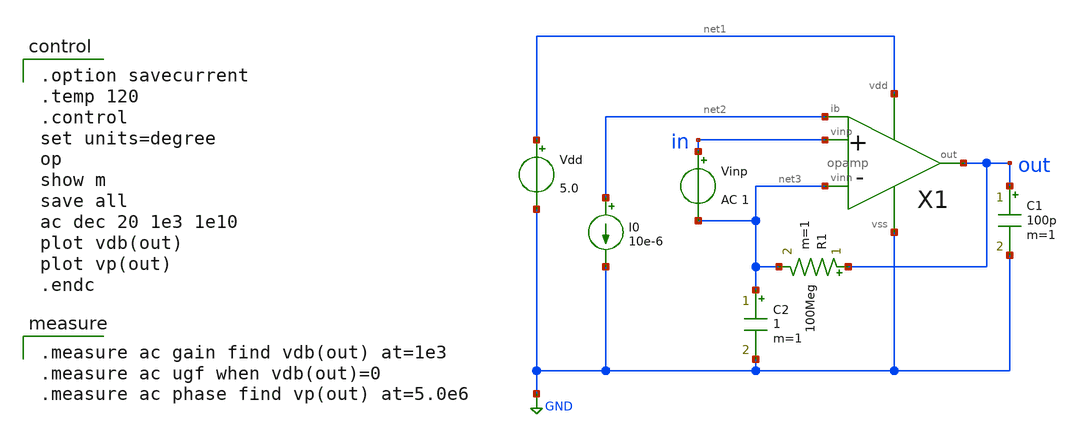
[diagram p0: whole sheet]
** sch_path: schematic/20250924_OSS_Workshop/ishikai/opamp/sample/opamp_ac_temp.sch
**.subckt opamp_ac_temp
Vdd net1 GND 5.0
C1 out GND 100p m=1
X1 in net3 net2 out net1 GND opamp
I0 net2 GND 10e-6
R1 out net3 100Meg m=1
C2 net3 GND 1 m=1
Vinp in net3 AC 1
**** begin user architecture code

.option savecurrent
.temp 120
.control
set units=degree
op
show m
save all
ac dec 20 1e3 1e10
plot vdb(out)
plot vp(out)
.endc


.measure ac gain find vdb(out) at=1e3
.measure ac ugf when vdb(out)=0
.measure ac phase find vp(out) at=5.0e6

 .include $::LIB/../ip62_models
**** end user architecture code
**.ends

* expanding   symbol:  opamp.sym # of pins=6
** sym_path: schematic/20250924_OSS_Workshop/ishikai/opamp/sample/opamp.sym
** sch_path: schematic/20250924_OSS_Workshop/ishikai/opamp/sample/opamp.sch
.subckt opamp vinp vinn ib out vdd vss
*.ipin vinp
*.ipin vinn
*.opin out
*.iopin vdd
*.iopin vss
*.iopin ib
X1 vinp vinn net2 vdd vss ib diff
X2 net2 ib out vdd vss cs
XM9 net1 ib vdd vdd PMOS w=30u l=1u as=0 ad=0 ps=0 pd=0 nrd=0 nrs=0 m=1
XM12 net3 net1 net2 vss NMOS w=20u l=1u as=0 ad=0 ps=0 pd=0 nrd=0 nrs=0 m=1
XM1 ib ib vdd vdd PMOS w=30u l=1u as=0 ad=0 ps=0 pd=0 nrd=0 nrs=0 m=1
XM10 net1 net1 net4 vss NMOS w=10u l=1u as=0 ad=0 ps=0 pd=0 nrd=0 nrs=0 m=1
XM11 net4 net4 vss vss NMOS w=10u l=1u as=0 ad=0 ps=0 pd=0 nrd=0 nrs=0 m=1
XC1 net3 out vss F_CSIO c=8.856p x=120u y=120u m=1
.ends


* expanding   symbol:  diff.sym # of pins=6
** sym_path: schematic/20250924_OSS_Workshop/ishikai/opamp/sample/diff.sym
** sch_path: schematic/20250924_OSS_Workshop/ishikai/opamp/sample/diff.sch
.subckt diff vinp vinn out vdd vss vb
*.ipin vinn
*.ipin vinp
*.ipin vb
*.opin out
*.iopin vdd
*.iopin vss
XM5 net2 vb vdd vdd PMOS w=180u l=1u as=0 ad=0 ps=0 pd=0 nrd=0 nrs=0 m=1
XM1 net1 vinn net2 net2 PMOS w=360u l=1u as=0 ad=0 ps=0 pd=0 nrd=0 nrs=0 m=1
XM2 out vinp net2 net2 PMOS w=360u l=1u as=0 ad=0 ps=0 pd=0 nrd=0 nrs=0 m=1
XM3 net1 net1 vss vss NMOS w=30u l=1u as=0 ad=0 ps=0 pd=0 nrd=0 nrs=0 m=1
XM4 out net1 vss vss NMOS w=30u l=1u as=0 ad=0 ps=0 pd=0 nrd=0 nrs=0 m=1
.ends


* expanding   symbol:  cs.sym # of pins=5
** sym_path: schematic/20250924_OSS_Workshop/ishikai/opamp/sample/cs.sym
** sch_path: schematic/20250924_OSS_Workshop/ishikai/opamp/sample/cs.sch
.subckt cs vin vb out vdd vss
*.ipin vb
*.ipin vin
*.opin out
*.iopin vss
*.iopin vdd
XM6 out vb vdd vdd PMOS w=270u l=1u as=0 ad=0 ps=0 pd=0 nrd=0 nrs=0 m=1
XM7 out vin vss vss NMOS w=90u l=1u as=0 ad=0 ps=0 pd=0 nrd=0 nrs=0 m=1
.ends

.GLOBAL GND
.end
